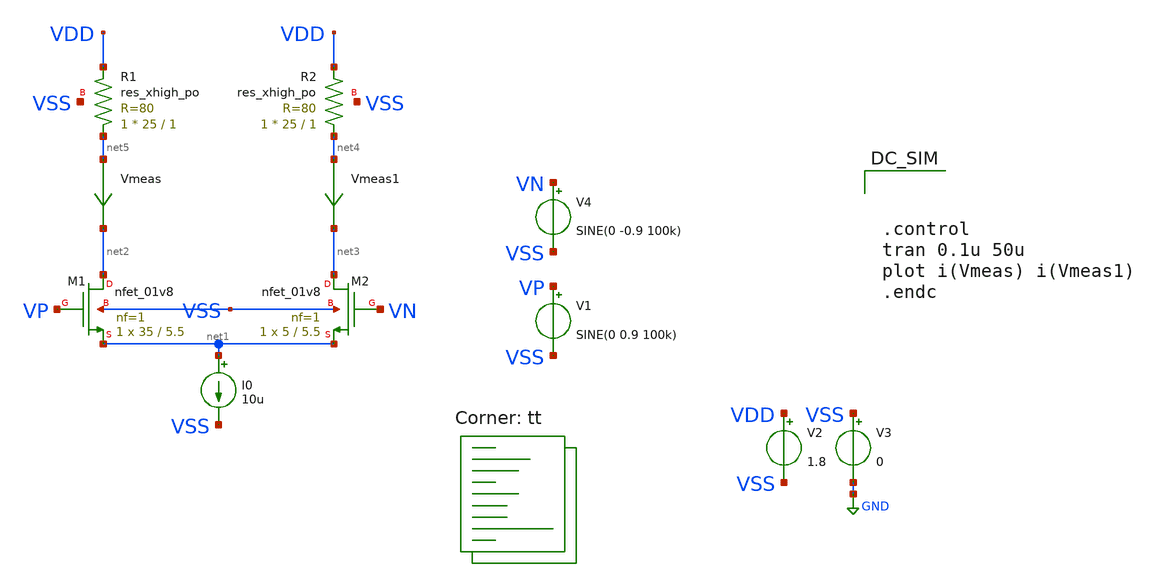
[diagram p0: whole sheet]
** sch_path: designs/libs/core_analog/p-ota/examples/fet-tb/diffpair.sch
**.subckt diffpair
XM2 net3 VN net1 VSS sky130_fd_pr__nfet_01v8 L=5.5 W=5 nf=1 ad='int((nf+1)/2) * W/nf * 0.29' as='int((nf+2)/2) * W/nf * 0.29'
+ pd='2*int((nf+1)/2) * (W/nf + 0.29)' ps='2*int((nf+2)/2) * (W/nf + 0.29)' nrd='0.29 / W' nrs='0.29 / W'
+ sa=0 sb=0 sd=0 mult=1 m=1
XM1 net2 VP net1 VSS sky130_fd_pr__nfet_01v8 L=5.5 W=35 nf=1 ad='int((nf+1)/2) * W/nf * 0.29' as='int((nf+2)/2) * W/nf * 0.29'
+ pd='2*int((nf+1)/2) * (W/nf + 0.29)' ps='2*int((nf+2)/2) * (W/nf + 0.29)' nrd='0.29 / W' nrs='0.29 / W'
+ sa=0 sb=0 sd=0 mult=1 m=1
XR1 net5 VDD VSS sky130_fd_pr__res_xhigh_po W=25 L=1 mult=1 m=1
XR2 net4 VDD VSS sky130_fd_pr__res_xhigh_po W=25 L=1 mult=1 m=1
V1 VP VSS SINE(0 0.9 100k)
V2 VDD VSS 1.8
V3 VSS GND 0
I0 net1 VSS 10u
V4 VN VSS SINE(0 -0.9 100k)
Vmeas net5 net2 0
.save i(vmeas)
Vmeas1 net4 net3 0
.save i(vmeas1)
**** begin user architecture code
.lib $::SKYWATER_MODELS/sky130.lib.spice tt



.control
tran 0.1u 50u
plot i(Vmeas) i(Vmeas1)
.endc

**** end user architecture code
**.ends
.GLOBAL GND
.end
